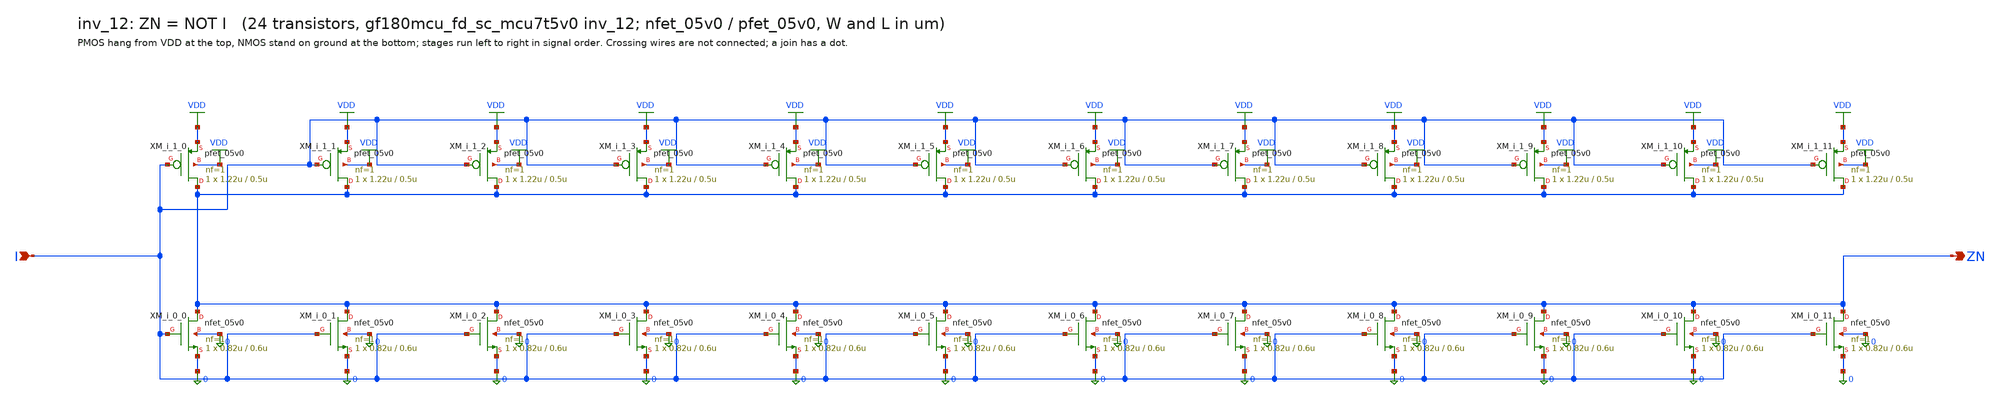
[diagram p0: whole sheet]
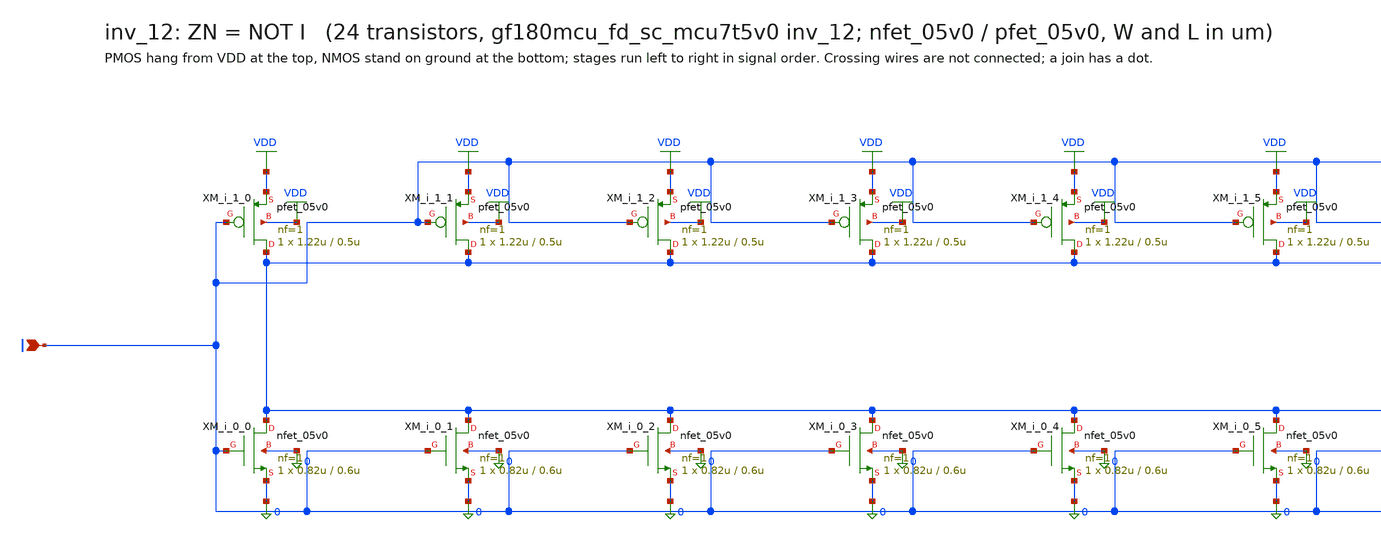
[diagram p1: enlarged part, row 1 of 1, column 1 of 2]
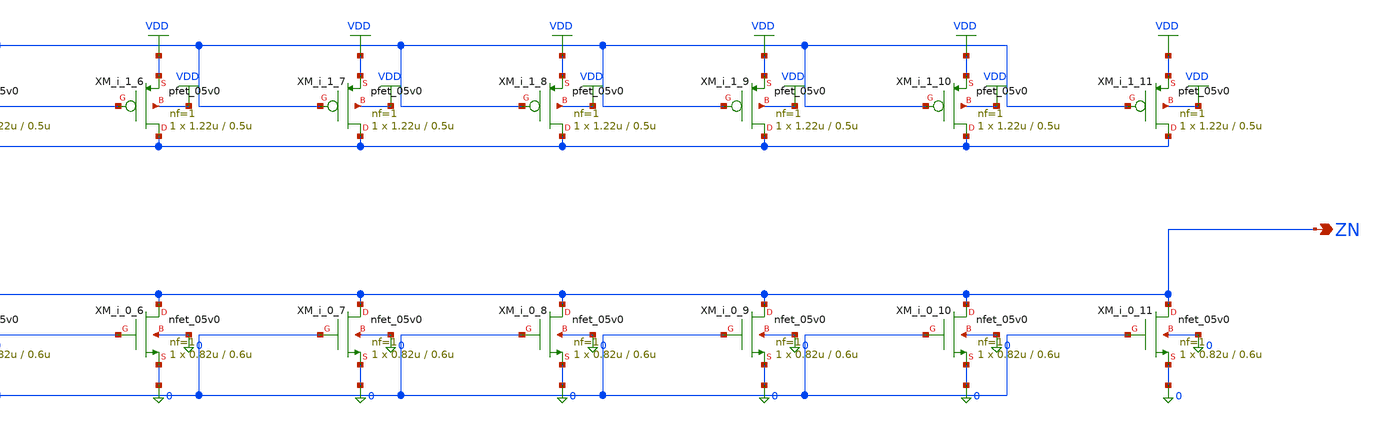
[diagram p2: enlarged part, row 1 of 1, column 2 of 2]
** sch_path: xschem/cells_tx/inv_12.sch
**.subckt inv_12 I ZN
*.ipin I
*.opin ZN
XM_i_0_0 ZN I 0 0 nfet_05v0 L=0.6u W=0.82u nf=1 ad=4.1e-13 as=4.1e-13 pd=2.64e-06 ps=2.64e-06 nrd=0
+ nrs=0 sa=0 sb=0 sd=0 m=1
XM_i_0_1 ZN I 0 0 nfet_05v0 L=0.6u W=0.82u nf=1 ad=4.1e-13 as=4.1e-13 pd=2.64e-06 ps=2.64e-06 nrd=0
+ nrs=0 sa=0 sb=0 sd=0 m=1
XM_i_0_2 ZN I 0 0 nfet_05v0 L=0.6u W=0.82u nf=1 ad=4.1e-13 as=4.1e-13 pd=2.64e-06 ps=2.64e-06 nrd=0
+ nrs=0 sa=0 sb=0 sd=0 m=1
XM_i_0_3 ZN I 0 0 nfet_05v0 L=0.6u W=0.82u nf=1 ad=4.1e-13 as=4.1e-13 pd=2.64e-06 ps=2.64e-06 nrd=0
+ nrs=0 sa=0 sb=0 sd=0 m=1
XM_i_0_4 ZN I 0 0 nfet_05v0 L=0.6u W=0.82u nf=1 ad=4.1e-13 as=4.1e-13 pd=2.64e-06 ps=2.64e-06 nrd=0
+ nrs=0 sa=0 sb=0 sd=0 m=1
XM_i_0_5 ZN I 0 0 nfet_05v0 L=0.6u W=0.82u nf=1 ad=4.1e-13 as=4.1e-13 pd=2.64e-06 ps=2.64e-06 nrd=0
+ nrs=0 sa=0 sb=0 sd=0 m=1
XM_i_0_6 ZN I 0 0 nfet_05v0 L=0.6u W=0.82u nf=1 ad=4.1e-13 as=4.1e-13 pd=2.64e-06 ps=2.64e-06 nrd=0
+ nrs=0 sa=0 sb=0 sd=0 m=1
XM_i_0_7 ZN I 0 0 nfet_05v0 L=0.6u W=0.82u nf=1 ad=4.1e-13 as=4.1e-13 pd=2.64e-06 ps=2.64e-06 nrd=0
+ nrs=0 sa=0 sb=0 sd=0 m=1
XM_i_0_8 ZN I 0 0 nfet_05v0 L=0.6u W=0.82u nf=1 ad=4.1e-13 as=4.1e-13 pd=2.64e-06 ps=2.64e-06 nrd=0
+ nrs=0 sa=0 sb=0 sd=0 m=1
XM_i_0_9 ZN I 0 0 nfet_05v0 L=0.6u W=0.82u nf=1 ad=4.1e-13 as=4.1e-13 pd=2.64e-06 ps=2.64e-06 nrd=0
+ nrs=0 sa=0 sb=0 sd=0 m=1
XM_i_0_10 ZN I 0 0 nfet_05v0 L=0.6u W=0.82u nf=1 ad=4.1e-13 as=4.1e-13 pd=2.64e-06 ps=2.64e-06 nrd=0
+ nrs=0 sa=0 sb=0 sd=0 m=1
XM_i_0_11 ZN I 0 0 nfet_05v0 L=0.6u W=0.82u nf=1 ad=4.1e-13 as=4.1e-13 pd=2.64e-06 ps=2.64e-06 nrd=0
+ nrs=0 sa=0 sb=0 sd=0 m=1
XM_i_1_0 ZN I VDD VDD pfet_05v0 L=0.5u W=1.22u nf=1 ad=6.1e-13 as=6.1e-13 pd=3.44e-06 ps=3.44e-06
+ nrd=0 nrs=0 sa=0 sb=0 sd=0 m=1
XM_i_1_1 ZN I VDD VDD pfet_05v0 L=0.5u W=1.22u nf=1 ad=6.1e-13 as=6.1e-13 pd=3.44e-06 ps=3.44e-06
+ nrd=0 nrs=0 sa=0 sb=0 sd=0 m=1
XM_i_1_2 ZN I VDD VDD pfet_05v0 L=0.5u W=1.22u nf=1 ad=6.1e-13 as=6.1e-13 pd=3.44e-06 ps=3.44e-06
+ nrd=0 nrs=0 sa=0 sb=0 sd=0 m=1
XM_i_1_3 ZN I VDD VDD pfet_05v0 L=0.5u W=1.22u nf=1 ad=6.1e-13 as=6.1e-13 pd=3.44e-06 ps=3.44e-06
+ nrd=0 nrs=0 sa=0 sb=0 sd=0 m=1
XM_i_1_4 ZN I VDD VDD pfet_05v0 L=0.5u W=1.22u nf=1 ad=6.1e-13 as=6.1e-13 pd=3.44e-06 ps=3.44e-06
+ nrd=0 nrs=0 sa=0 sb=0 sd=0 m=1
XM_i_1_5 ZN I VDD VDD pfet_05v0 L=0.5u W=1.22u nf=1 ad=6.1e-13 as=6.1e-13 pd=3.44e-06 ps=3.44e-06
+ nrd=0 nrs=0 sa=0 sb=0 sd=0 m=1
XM_i_1_6 ZN I VDD VDD pfet_05v0 L=0.5u W=1.22u nf=1 ad=6.1e-13 as=6.1e-13 pd=3.44e-06 ps=3.44e-06
+ nrd=0 nrs=0 sa=0 sb=0 sd=0 m=1
XM_i_1_7 ZN I VDD VDD pfet_05v0 L=0.5u W=1.22u nf=1 ad=6.1e-13 as=6.1e-13 pd=3.44e-06 ps=3.44e-06
+ nrd=0 nrs=0 sa=0 sb=0 sd=0 m=1
XM_i_1_8 ZN I VDD VDD pfet_05v0 L=0.5u W=1.22u nf=1 ad=6.1e-13 as=6.1e-13 pd=3.44e-06 ps=3.44e-06
+ nrd=0 nrs=0 sa=0 sb=0 sd=0 m=1
XM_i_1_9 ZN I VDD VDD pfet_05v0 L=0.5u W=1.22u nf=1 ad=6.1e-13 as=6.1e-13 pd=3.44e-06 ps=3.44e-06
+ nrd=0 nrs=0 sa=0 sb=0 sd=0 m=1
XM_i_1_10 ZN I VDD VDD pfet_05v0 L=0.5u W=1.22u nf=1 ad=6.1e-13 as=6.1e-13 pd=3.44e-06 ps=3.44e-06
+ nrd=0 nrs=0 sa=0 sb=0 sd=0 m=1
XM_i_1_11 ZN I VDD VDD pfet_05v0 L=0.5u W=1.22u nf=1 ad=6.1e-13 as=6.1e-13 pd=3.44e-06 ps=3.44e-06
+ nrd=0 nrs=0 sa=0 sb=0 sd=0 m=1
**.ends
.GLOBAL VDD
.end
